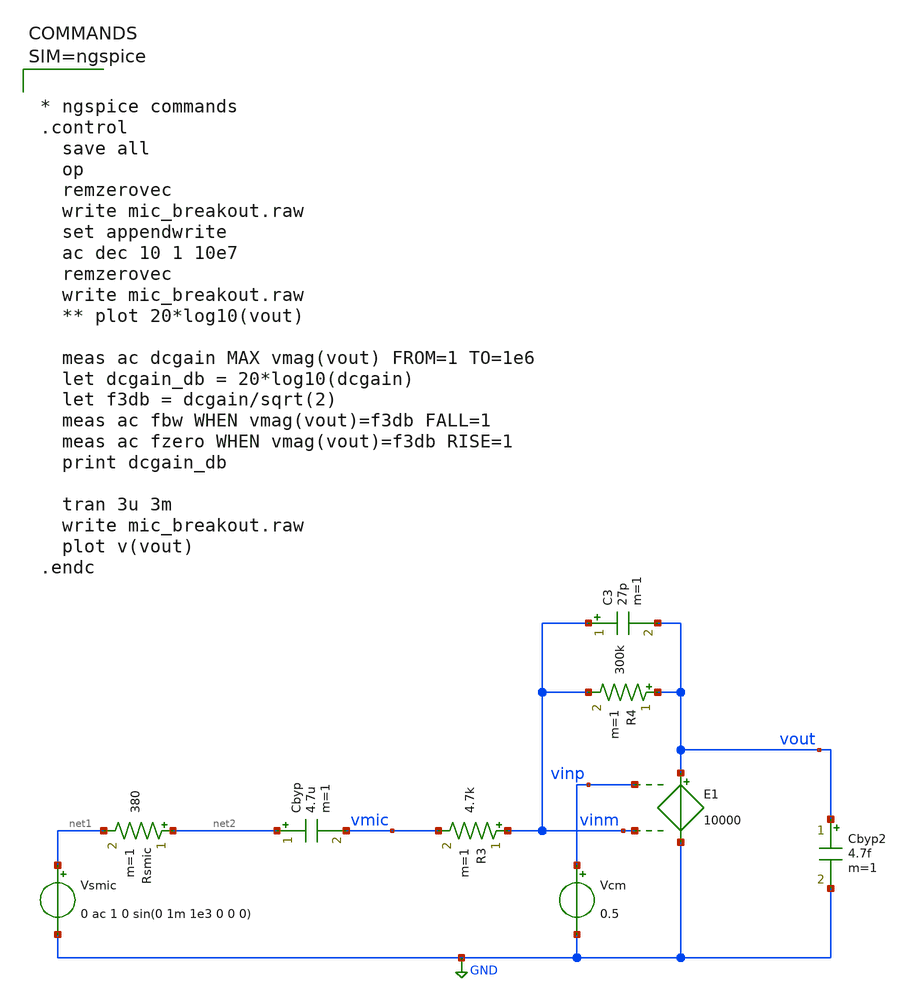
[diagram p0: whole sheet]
** sch_path: xschem/mic_breakout.sch
**.subckt mic_breakout
Vsmic net1 GND 0 ac 1 0 sin(0 1m 1e3 0 0 0)
Rsmic net2 net1 380 m=1
Cbyp net2 vmic 4.7u m=1
R3 vinm vmic 4.7k m=1
E1 vout GND vinp vinm 10000
Vcm vinp GND 0.5
R4 vout vinm 300k m=1
C3 vinm vout 27p m=1
Cbyp2 vout GND 4.7f m=1
**** begin user architecture code



* ngspice commands
.control
  save all
  op
  remzerovec
  write mic_breakout.raw
  set appendwrite
  ac dec 10 1 10e7
  remzerovec
  write mic_breakout.raw
  ** plot 20*log10(vout)

  meas ac dcgain MAX vmag(vout) FROM=1 TO=1e6
  let dcgain_db = 20*log10(dcgain)
  let f3db = dcgain/sqrt(2)
  meas ac fbw WHEN vmag(vout)=f3db FALL=1
  meas ac fzero WHEN vmag(vout)=f3db RISE=1
  print dcgain_db

  tran 3u 3m
  write mic_breakout.raw
  plot v(vout)
.endc



**** end user architecture code
**.ends
.GLOBAL GND
.end
